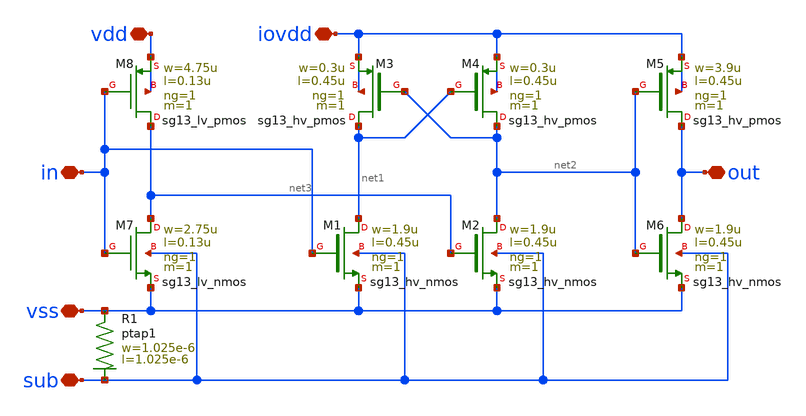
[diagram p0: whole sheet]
** sch_path: MSPHY6034-main/dependencies/unic_cass_2025_team04_padring/xschem/openpdk-libraries/ihp-sg13g2/sg13g2_io/xschem/sg13g2_LevelUpInv.sch
**.subckt sg13g2_LevelUpInv iovdd vss out in vdd sub
*.iopin iovdd
*.iopin vss
*.iopin out
*.iopin in
*.iopin vdd
*.iopin sub
XR1 vss sub ptap1 R=190.3 w=1.025e-6 l=1.025e-6
XM1 net1 in vss sub sg13_hv_nmos w=1.9u l=0.45u ng=1 m=1 mm_ok=1
XM3 net1 net2 iovdd iovdd sg13_hv_pmos w=0.3u l=0.45u ng=1 m=1 mm_ok=1
XM4 net2 net1 iovdd iovdd sg13_hv_pmos w=0.3u l=0.45u ng=1 m=1 mm_ok=1
XM5 out net2 iovdd iovdd sg13_hv_pmos w=3.9u l=0.45u ng=1 m=1 mm_ok=1
XM2 net2 net3 vss sub sg13_hv_nmos w=1.9u l=0.45u ng=1 m=1 mm_ok=1
XM6 out net2 vss sub sg13_hv_nmos w=1.9u l=0.45u ng=1 m=1 mm_ok=1
XM7 net3 in vss sub sg13_lv_nmos w=2.75u l=0.13u ng=1 m=1 mm_ok=1
XM8 net3 in vdd vdd sg13_lv_pmos w=4.75u l=0.13u ng=1 m=1 mm_ok=1
**.ends
.end
